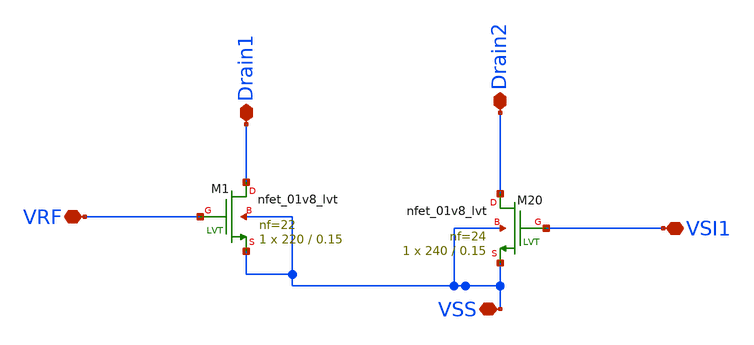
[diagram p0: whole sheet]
** sch_path: xschem/xschem4_sic_oct_20/interdigitezed_exmaple.sch
**.subckt interdigitezed_exmaple VRF VSI1 VSS Drain1 Drain2
*.iopin VRF
*.iopin VSI1
*.iopin VSS
*.iopin Drain1
*.iopin Drain2
XM1 Drain1 VRF VSS VSS sky130_fd_pr__nfet_01v8_lvt L=0.15 W=220 nf=22 ad='int((nf+1)/2) * W/nf * 0.29'
+ as='int((nf+2)/2) * W/nf * 0.29' pd='2*int((nf+1)/2) * (W/nf + 0.29)' ps='2*int((nf+2)/2) * (W/nf + 0.29)'
+ nrd='0.29 / W' nrs='0.29 / W' sa=0 sb=0 sd=0 mult=1 m=1
XM20 Drain2 VSI1 VSS VSS sky130_fd_pr__nfet_01v8_lvt L=0.15 W=240 nf=24 ad='int((nf+1)/2) * W/nf * 0.29'
+ as='int((nf+2)/2) * W/nf * 0.29' pd='2*int((nf+1)/2) * (W/nf + 0.29)' ps='2*int((nf+2)/2) * (W/nf + 0.29)'
+ nrd='0.29 / W' nrs='0.29 / W' sa=0 sb=0 sd=0 mult=1 m=1
**.ends
.end
